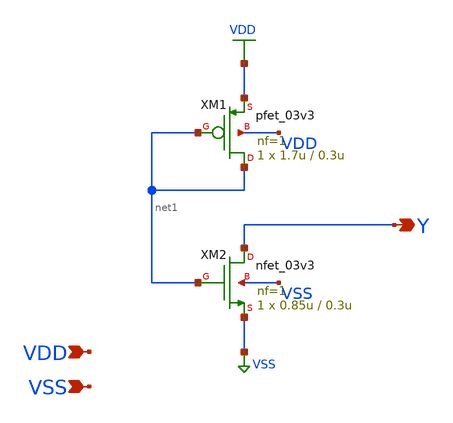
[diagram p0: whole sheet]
** sch_path: gf180mcu_osu_sc_gp9t3v3/xschem/gf180mcu_osu_sc_gp9t3v3__tiel.sch
**.subckt gf180mcu_osu_sc_gp9t3v3__tiel Y VDD VSS
*.opin Y
*.ipin VDD
*.ipin VSS
XM1 net1 net1 VDD VDD pfet_03v3 L=0.3u W=1.7u nf=1 ad='int((nf+1)/2) * W/nf * 0.18u' as='int((nf+2)/2) * W/nf * 0.18u'
+ pd='2*int((nf+1)/2) * (W/nf + 0.18u)' ps='2*int((nf+2)/2) * (W/nf + 0.18u)' nrd='0.18u / W' nrs='0.18u / W'
+ sa=0 sb=0 sd=0 m=1
XM2 Y net1 VSS VSS nfet_03v3 L=0.3u W=0.85u nf=1 ad='int((nf+1)/2) * W/nf * 0.18u' as='int((nf+2)/2) * W/nf * 0.18u'
+ pd='2*int((nf+1)/2) * (W/nf + 0.18u)' ps='2*int((nf+2)/2) * (W/nf + 0.18u)' nrd='0.18u / W' nrs='0.18u / W'
+ sa=0 sb=0 sd=0 m=1
**.ends
.GLOBAL VDD
.GLOBAL VSS
.end
